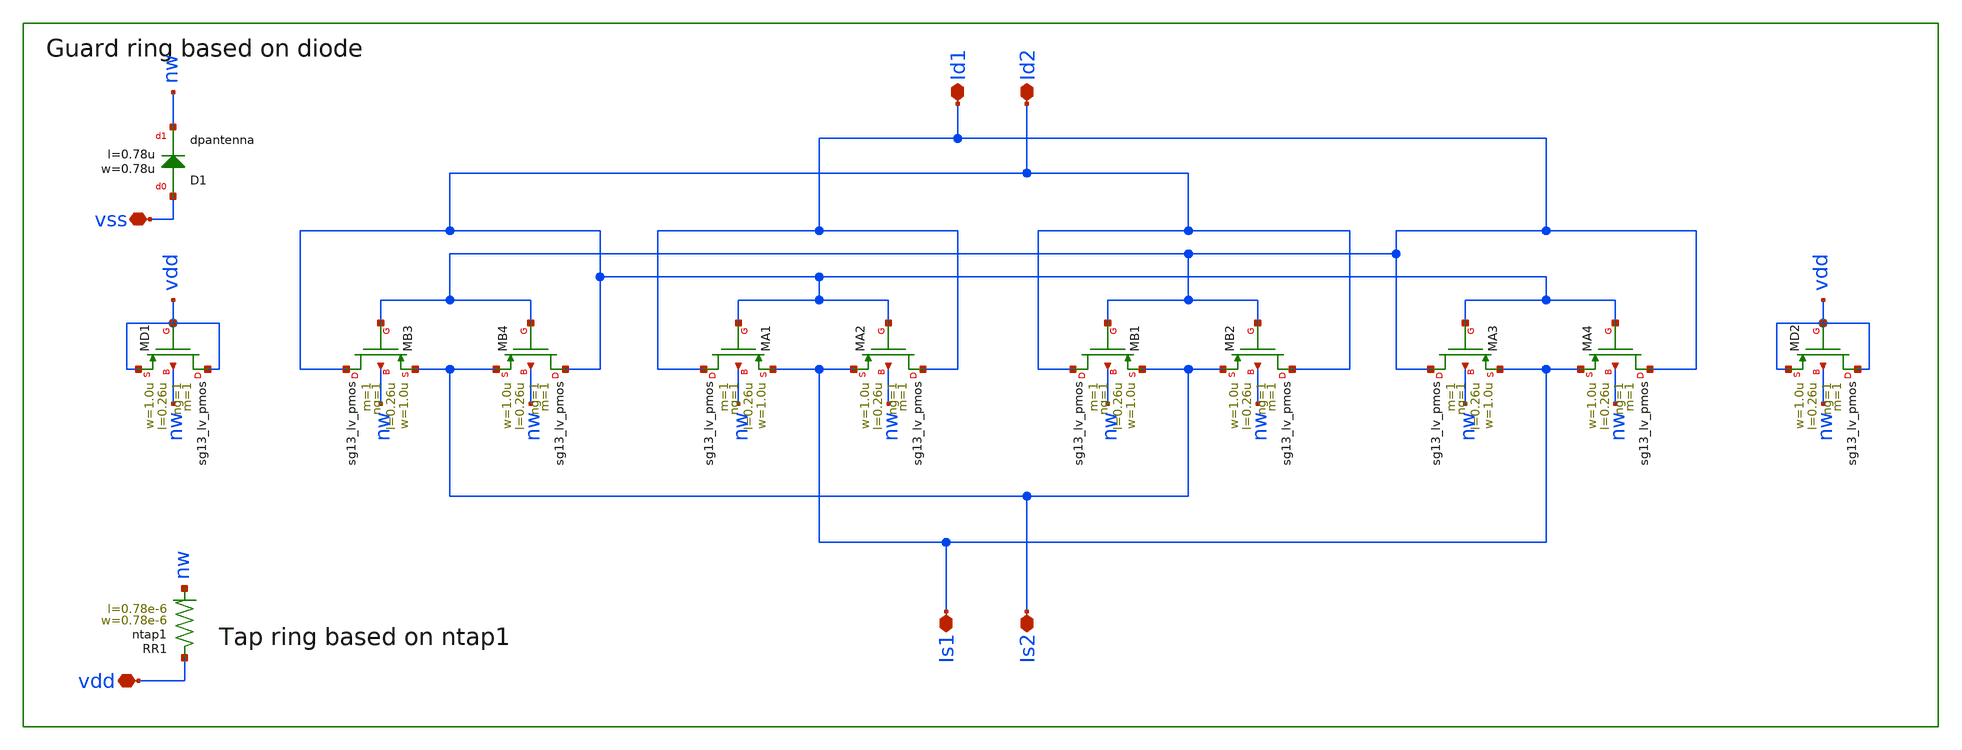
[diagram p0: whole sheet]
** sch_path: CMP7345-main/schematic/xschem/cc_pair_pmos.sch
**.subckt cc_pair_pmos vdd Id2 Id1 Is2 Is1 vss
*.iopin vdd
*.iopin Id2
*.iopin Id1
*.iopin Is2
*.iopin Is1
*.iopin vss
XMA1 Id1 Id2 Is1 nw sg13_lv_pmos w=1.0u l=0.26u ng=1 m=1 mm_ok=0
XMB1 Id2 Id1 Is2 nw sg13_lv_pmos w=1.0u l=0.26u ng=1 m=1 mm_ok=0
XMA2 Id1 Id2 Is1 nw sg13_lv_pmos w=1.0u l=0.26u ng=1 m=1 mm_ok=0
XMB2 Id2 Id1 Is2 nw sg13_lv_pmos w=1.0u l=0.26u ng=1 m=1 mm_ok=0
XMA3 Id1 Id2 Is1 nw sg13_lv_pmos w=1.0u l=0.26u ng=1 m=1 mm_ok=0
XMA4 Id1 Id2 Is1 nw sg13_lv_pmos w=1.0u l=0.26u ng=1 m=1 mm_ok=0
XMB3 Id2 Id1 Is2 nw sg13_lv_pmos w=1.0u l=0.26u ng=1 m=1 mm_ok=0
XMB4 Id2 Id1 Is2 nw sg13_lv_pmos w=1.0u l=0.26u ng=1 m=1 mm_ok=0
XMD1 vdd vdd vdd nw sg13_lv_pmos w=1.0u l=0.26u ng=1 m=1 mm_ok=0
XMD2 vdd vdd vdd nw sg13_lv_pmos w=1.0u l=0.26u ng=1 m=1 mm_ok=0
XD1 vss nw dpantenna l=0.78u w=0.78u
XR1 vdd nw ntap1 R=262.8 w=0.78e-6 l=0.78e-6
**.ends
.end
